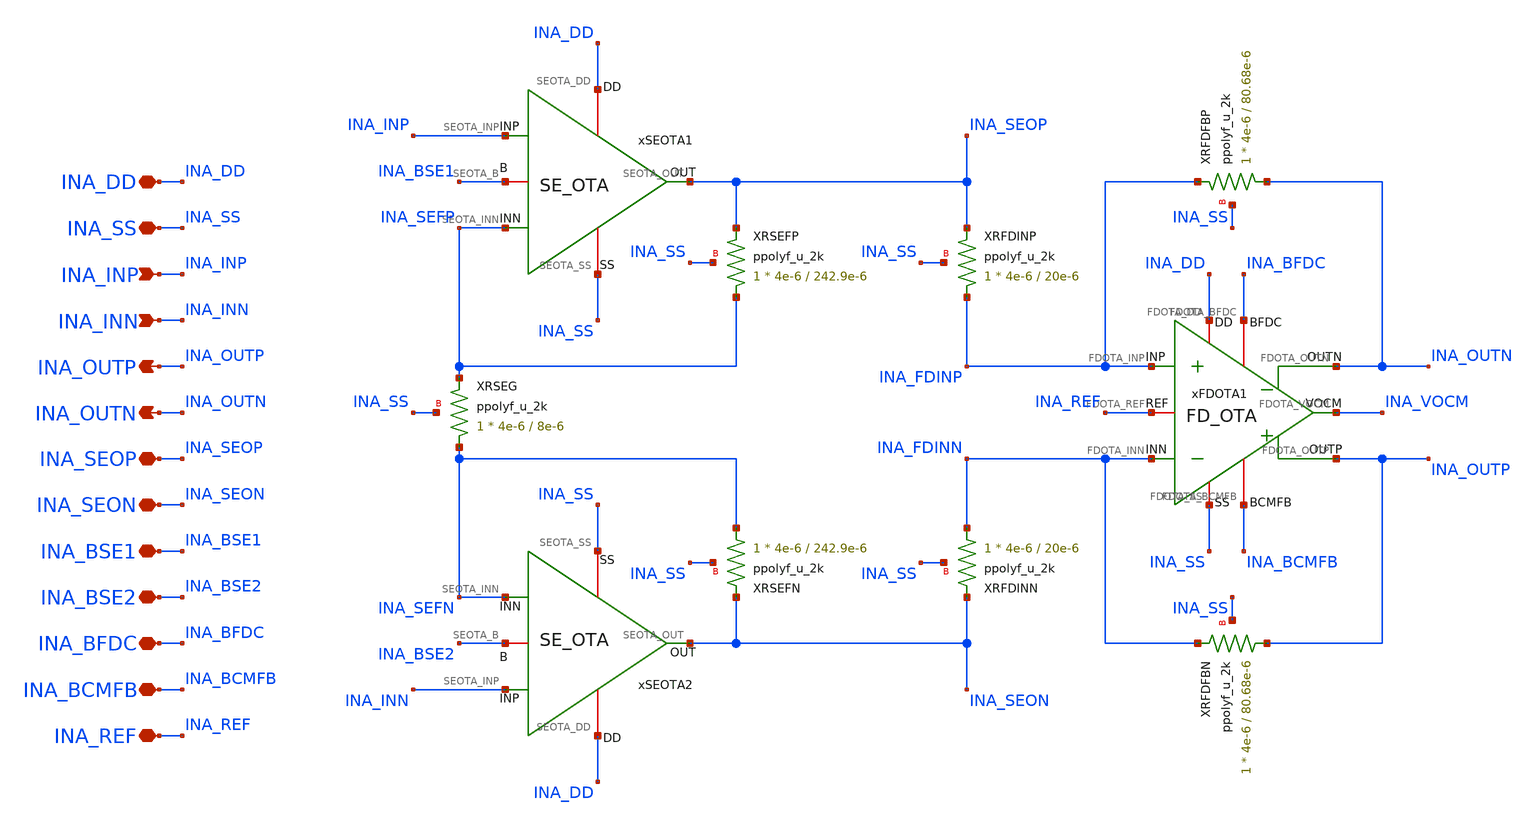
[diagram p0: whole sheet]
** sch_path: Design_Files/IC Design/Schematic/AFE_BLOCKS/INA/INA.sch
**.subckt INA INA_DD INA_SS INA_INP INA_INN INA_OUTP INA_BFDC INA_OUTN INA_BCMFB INA_REF INA_BSE1
*+ INA_SEON INA_SEOP INA_BSE2
*.iopin INA_DD
*.iopin INA_SS
*.ipin INA_INP
*.ipin INA_INN
*.opin INA_OUTP
*.iopin INA_BFDC
*.opin INA_OUTN
*.iopin INA_BCMFB
*.iopin INA_REF
*.iopin INA_BSE1
*.iopin INA_SEON
*.iopin INA_SEOP
*.iopin INA_BSE2
xFDOTA1 INA_DD INA_SS INA_FDINP INA_FDINN INA_OUTN INA_BFDC INA_OUTP INA_BCMFB INA_REF INA_VOCM
+ FD_OTA
xSEOTA1 INA_DD INA_SS INA_INP INA_SEFP INA_SEOP INA_BSE1 SE_OTA
xSEOTA2 INA_DD INA_SS INA_INN INA_SEFN INA_SEON INA_BSE2 SE_OTA
XRFDFBP INA_OUTN INA_FDINP INA_SS ppolyf_u_2k r_width=4e-6 r_length=80.68e-6 m=1
XRFDFBN INA_OUTP INA_FDINN INA_SS ppolyf_u_2k r_width=4e-6 r_length=80.68e-6 m=1
XRFDINP INA_FDINP INA_SEOP INA_SS ppolyf_u_2k r_width=4e-6 r_length=20e-6 m=1
XRFDINN INA_FDINN INA_SEON INA_SS ppolyf_u_2k r_width=4e-6 r_length=20e-6 m=1
XRSEFP INA_SEFP INA_SEOP INA_SS ppolyf_u_2k r_width=4e-6 r_length=242.9e-6 m=1
XRSEFN INA_SEFN INA_SEON INA_SS ppolyf_u_2k r_width=4e-6 r_length=242.9e-6 m=1
XRSEG INA_SEFN INA_SEFP INA_SS ppolyf_u_2k r_width=4e-6 r_length=8e-6 m=1
**.ends
.end
